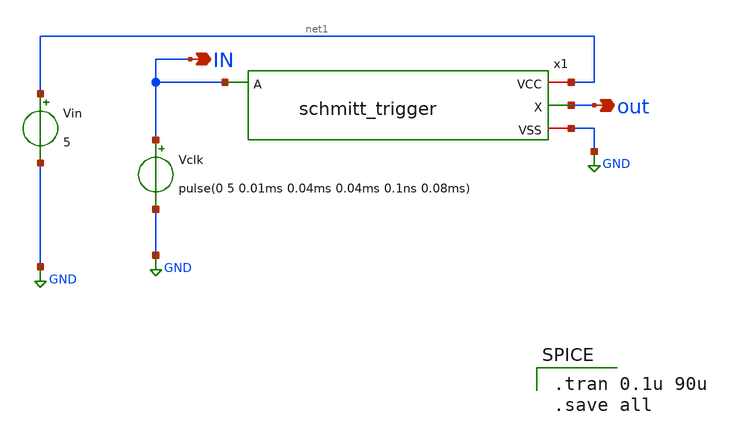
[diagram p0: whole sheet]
** sch_path: DISEÑO/ANALOGICO/V;SI/ST/xschem/schmitt_trigger_TB.sch
**.subckt schmitt_trigger_TB out IN
*.opin out
*.opin IN
Vclk IN GND pulse(0 5 0.01ms 0.04ms 0.04ms 0.1ns 0.08ms)
Vin net1 GND 5
x1 net1 IN out GND schmitt_trigger
**** begin user architecture code

.tran 0.1u 90u
.save all


** opencircuitdesign pdks install
.lib $::SKYWATER_MODELS/sky130.lib.spice tt


**** end user architecture code
**.ends

* expanding   symbol:  schmitt_trigger.sym # of pins=4
** sym_path: DISEÑO/ANALOGICO/V;SI/ST/xschem/schmitt_trigger.sym
** sch_path: DISEÑO/ANALOGICO/V;SI/ST/xschem/schmitt_trigger.sch
.subckt schmitt_trigger VCC A X VSS
*.ipin A
*.opin X
*.iopin VSS
*.iopin VCC
XM0 net1 A net2 VCC sky130_fd_pr__pfet_g5v0d10v5 L=0.5 W=0.75 nf=1 ad='int((nf+1)/2) * W/nf * 0.29' as='int((nf+2)/2) * W/nf * 0.29'
+ pd='2*int((nf+1)/2) * (W/nf + 0.29)' ps='2*int((nf+2)/2) * (W/nf + 0.29)' nrd='0.29 / W' nrs='0.29 / W'
+ sa=0 sb=0 sd=0 mult=1 m=1
XM1 net3 A net2 VSS sky130_fd_pr__nfet_g5v0d10v5 L=0.5 W=0.42 nf=1 ad='int((nf+1)/2) * W/nf * 0.29' as='int((nf+2)/2) * W/nf * 0.29'
+ pd='2*int((nf+1)/2) * (W/nf + 0.29)' ps='2*int((nf+2)/2) * (W/nf + 0.29)' nrd='0.29 / W' nrs='0.29 / W'
+ sa=0 sb=0 sd=0 mult=1 m=1
XM7 X net2 VCC VCC sky130_fd_pr__pfet_g5v0d10v5 L=0.5 W=1.5 nf=1 ad='int((nf+1)/2) * W/nf * 0.29' as='int((nf+2)/2) * W/nf * 0.29'
+ pd='2*int((nf+1)/2) * (W/nf + 0.29)' ps='2*int((nf+2)/2) * (W/nf + 0.29)' nrd='0.29 / W' nrs='0.29 / W'
+ sa=0 sb=0 sd=0 mult=1 m=1
XM6 X net2 VSS VSS sky130_fd_pr__nfet_g5v0d10v5 L=0.5 W=0.75 nf=1 ad='int((nf+1)/2) * W/nf * 0.29' as='int((nf+2)/2) * W/nf * 0.29'
+ pd='2*int((nf+1)/2) * (W/nf + 0.29)' ps='2*int((nf+2)/2) * (W/nf + 0.29)' nrd='0.29 / W' nrs='0.29 / W'
+ sa=0 sb=0 sd=0 mult=1 m=1
XM4 VCC A net1 VCC sky130_fd_pr__pfet_g5v0d10v5 L=0.5 W=0.75 nf=1 ad='int((nf+1)/2) * W/nf * 0.29' as='int((nf+2)/2) * W/nf * 0.29'
+ pd='2*int((nf+1)/2) * (W/nf + 0.29)' ps='2*int((nf+2)/2) * (W/nf + 0.29)' nrd='0.29 / W' nrs='0.29 / W'
+ sa=0 sb=0 sd=0 mult=1 m=1
XM5 net3 net2 net5 VSS sky130_fd_pr__nfet_g5v0d10v5 L=0.5 W=0.42 nf=1 ad='int((nf+1)/2) * W/nf * 0.29'
+ as='int((nf+2)/2) * W/nf * 0.29' pd='2*int((nf+1)/2) * (W/nf + 0.29)' ps='2*int((nf+2)/2) * (W/nf + 0.29)'
+ nrd='0.29 / W' nrs='0.29 / W' sa=0 sb=0 sd=0 mult=1 m=1
XM9 net1 net2 net4 VCC sky130_fd_pr__pfet_g5v0d10v5 L=0.5 W=0.75 nf=1 ad='int((nf+1)/2) * W/nf * 0.29'
+ as='int((nf+2)/2) * W/nf * 0.29' pd='2*int((nf+1)/2) * (W/nf + 0.29)' ps='2*int((nf+2)/2) * (W/nf + 0.29)'
+ nrd='0.29 / W' nrs='0.29 / W' sa=0 sb=0 sd=0 mult=1 m=1
XM8 VSS A net3 VSS sky130_fd_pr__nfet_g5v0d10v5 L=0.5 W=0.42 nf=1 ad='int((nf+1)/2) * W/nf * 0.29' as='int((nf+2)/2) * W/nf * 0.29'
+ pd='2*int((nf+1)/2) * (W/nf + 0.29)' ps='2*int((nf+2)/2) * (W/nf + 0.29)' nrd='0.29 / W' nrs='0.29 / W'
+ sa=0 sb=0 sd=0 mult=1 m=1
XX2 VSS net4 VSS sky130_fd_pr__res_generic_nd__hv W=0.29 L=1.355 mult=1 m=1
XX3 net5 VCC VCC sky130_fd_pr__res_generic_pd__hv W=0.29 L=3.11 mult=1 m=1
.ends

.GLOBAL GND
.end
